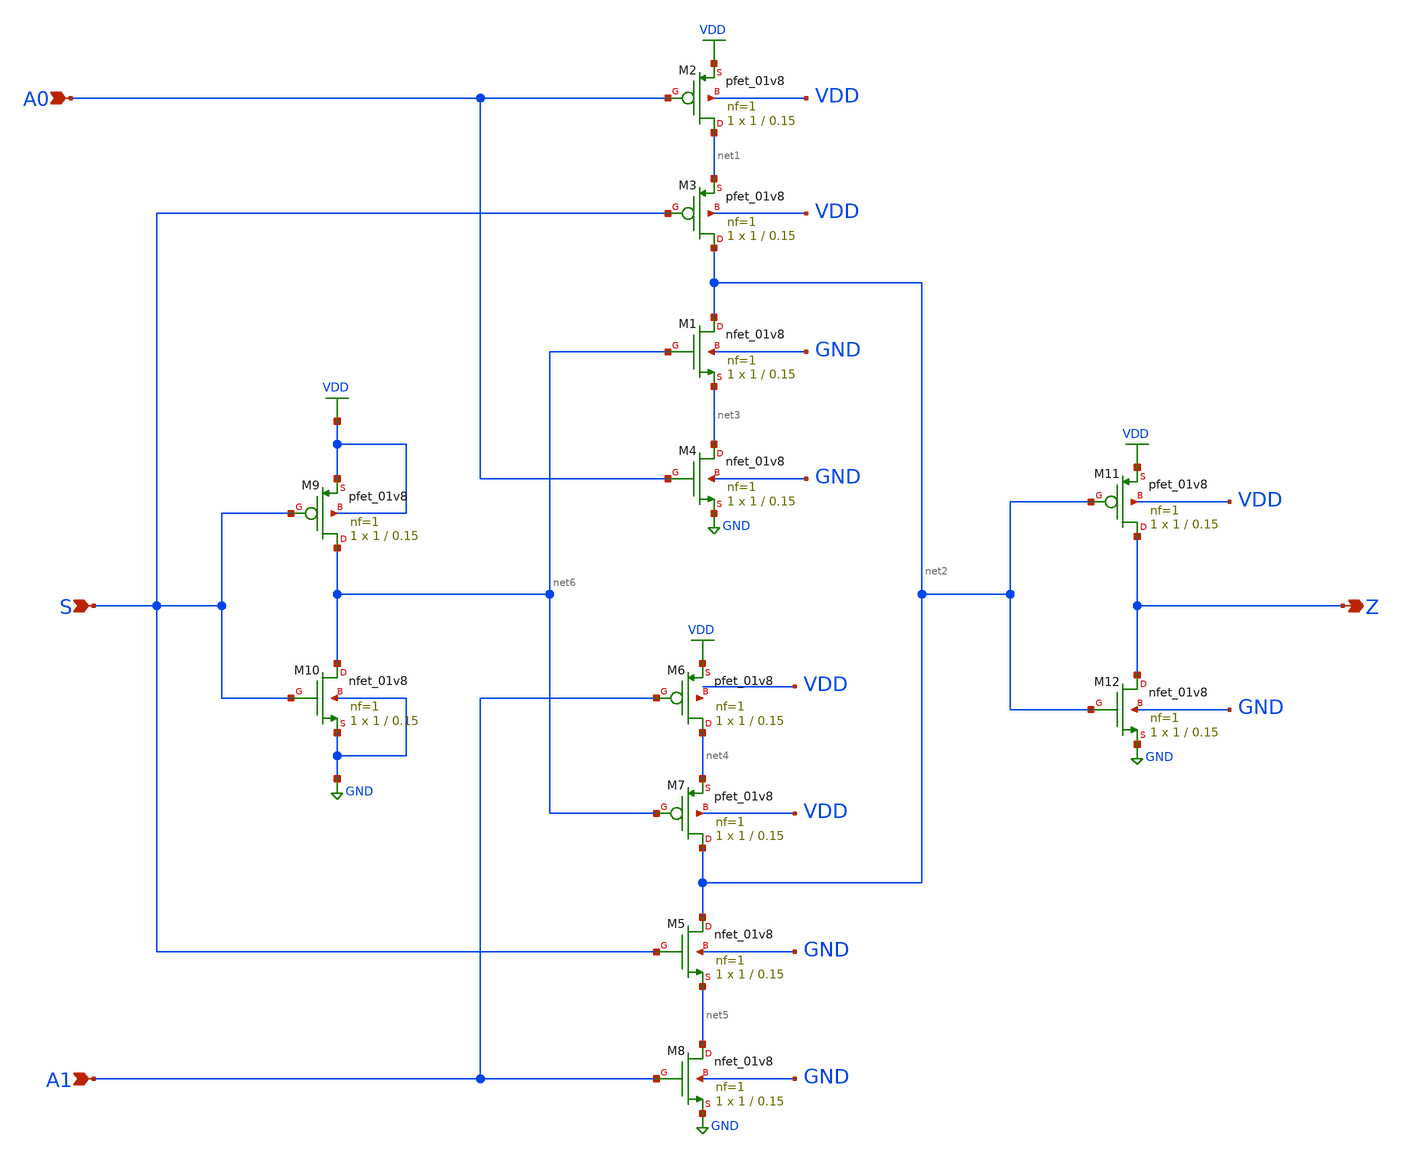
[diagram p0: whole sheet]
** sch_path: multiplexer/multiplexer.sch
**.subckt multiplexer A0 S A1 Z
*.ipin A0
*.ipin S
*.ipin A1
*.opin Z
XM1 net2 net6 net3 GND sky130_fd_pr__nfet_01v8 L=0.15 W=1 nf=1 ad='int((1 + 1)/2) * 1 / 1 * 0.29' as='int((1 + 2)/2) * 1 / 1 * 0.29'
+ pd='2*int((1 + 1)/2) * (1 / 1 + 0.29)' ps='2*int((1 + 2)/2) * (1 / 1 + 0.29)' nrd='0.29 / 1 ' nrs='0.29 / 1 '
+ sa=0 sb=0 sd=0 mult=1 m=1
XM2 net1 A0 VDD VDD sky130_fd_pr__pfet_01v8 L=0.15 W=1 nf=1 ad='int((1 + 1)/2) * 1 / 1 * 0.29' as='int((1 + 2)/2) * 1 / 1 * 0.29'
+ pd='2*int((1 + 1)/2) * (1 / 1 + 0.29)' ps='2*int((1 + 2)/2) * (1 / 1 + 0.29)' nrd='0.29 / 1 ' nrs='0.29 / 1 '
+ sa=0 sb=0 sd=0 mult=1 m=1
XM3 net2 S net1 VDD sky130_fd_pr__pfet_01v8 L=0.15 W=1 nf=1 ad='int((1 + 1)/2) * 1 / 1 * 0.29' as='int((1 + 2)/2) * 1 / 1 * 0.29'
+ pd='2*int((1 + 1)/2) * (1 / 1 + 0.29)' ps='2*int((1 + 2)/2) * (1 / 1 + 0.29)' nrd='0.29 / 1 ' nrs='0.29 / 1 '
+ sa=0 sb=0 sd=0 mult=1 m=1
XM4 net3 A0 GND GND sky130_fd_pr__nfet_01v8 L=0.15 W=1 nf=1 ad='int((1 + 1)/2) * 1 / 1 * 0.29' as='int((1 + 2)/2) * 1 / 1 * 0.29'
+ pd='2*int((1 + 1)/2) * (1 / 1 + 0.29)' ps='2*int((1 + 2)/2) * (1 / 1 + 0.29)' nrd='0.29 / 1 ' nrs='0.29 / 1 '
+ sa=0 sb=0 sd=0 mult=1 m=1
XM5 net2 S net5 GND sky130_fd_pr__nfet_01v8 L=0.15 W=1 nf=1 ad='int((1 + 1)/2) * 1 / 1 * 0.29' as='int((1 + 2)/2) * 1 / 1 * 0.29'
+ pd='2*int((1 + 1)/2) * (1 / 1 + 0.29)' ps='2*int((1 + 2)/2) * (1 / 1 + 0.29)' nrd='0.29 / 1 ' nrs='0.29 / 1 '
+ sa=0 sb=0 sd=0 mult=1 m=1
XM6 net4 A1 VDD net7 sky130_fd_pr__pfet_01v8 L=0.15 W=1 nf=1 ad='int((1 + 1)/2) * 1 / 1 * 0.29' as='int((1 + 2)/2) * 1 / 1 * 0.29'
+ pd='2*int((1 + 1)/2) * (1 / 1 + 0.29)' ps='2*int((1 + 2)/2) * (1 / 1 + 0.29)' nrd='0.29 / 1 ' nrs='0.29 / 1 '
+ sa=0 sb=0 sd=0 mult=1 m=1
XM7 net2 net6 net4 VDD sky130_fd_pr__pfet_01v8 L=0.15 W=1 nf=1 ad='int((1 + 1)/2) * 1 / 1 * 0.29' as='int((1 + 2)/2) * 1 / 1 * 0.29'
+ pd='2*int((1 + 1)/2) * (1 / 1 + 0.29)' ps='2*int((1 + 2)/2) * (1 / 1 + 0.29)' nrd='0.29 / 1 ' nrs='0.29 / 1 '
+ sa=0 sb=0 sd=0 mult=1 m=1
XM8 net5 A1 GND GND sky130_fd_pr__nfet_01v8 L=0.15 W=1 nf=1 ad='int((1 + 1)/2) * 1 / 1 * 0.29' as='int((1 + 2)/2) * 1 / 1 * 0.29'
+ pd='2*int((1 + 1)/2) * (1 / 1 + 0.29)' ps='2*int((1 + 2)/2) * (1 / 1 + 0.29)' nrd='0.29 / 1 ' nrs='0.29 / 1 '
+ sa=0 sb=0 sd=0 mult=1 m=1
XM9 net6 S VDD VDD sky130_fd_pr__pfet_01v8 L=0.15 W=1 nf=1 ad='int((1 + 1)/2) * 1 / 1 * 0.29' as='int((1 + 2)/2) * 1 / 1 * 0.29'
+ pd='2*int((1 + 1)/2) * (1 / 1 + 0.29)' ps='2*int((1 + 2)/2) * (1 / 1 + 0.29)' nrd='0.29 / 1 ' nrs='0.29 / 1 '
+ sa=0 sb=0 sd=0 mult=1 m=1
XM10 net6 S GND GND sky130_fd_pr__nfet_01v8 L=0.15 W=1 nf=1 ad='int((1 + 1)/2) * 1 / 1 * 0.29' as='int((1 + 2)/2) * 1 / 1 * 0.29'
+ pd='2*int((1 + 1)/2) * (1 / 1 + 0.29)' ps='2*int((1 + 2)/2) * (1 / 1 + 0.29)' nrd='0.29 / 1 ' nrs='0.29 / 1 '
+ sa=0 sb=0 sd=0 mult=1 m=1
XM11 Z net2 VDD VDD sky130_fd_pr__pfet_01v8 L=0.15 W=1 nf=1 ad='int((1 + 1)/2) * 1 / 1 * 0.29' as='int((1 + 2)/2) * 1 / 1 * 0.29'
+ pd='2*int((1 + 1)/2) * (1 / 1 + 0.29)' ps='2*int((1 + 2)/2) * (1 / 1 + 0.29)' nrd='0.29 / 1 ' nrs='0.29 / 1 '
+ sa=0 sb=0 sd=0 mult=1 m=1
XM12 Z net2 GND GND sky130_fd_pr__nfet_01v8 L=0.15 W=1 nf=1 ad='int((1 + 1)/2) * 1 / 1 * 0.29' as='int((1 + 2)/2) * 1 / 1 * 0.29'
+ pd='2*int((1 + 1)/2) * (1 / 1 + 0.29)' ps='2*int((1 + 2)/2) * (1 / 1 + 0.29)' nrd='0.29 / 1 ' nrs='0.29 / 1 '
+ sa=0 sb=0 sd=0 mult=1 m=1
**.ends
.GLOBAL GND
.GLOBAL VDD
.end
